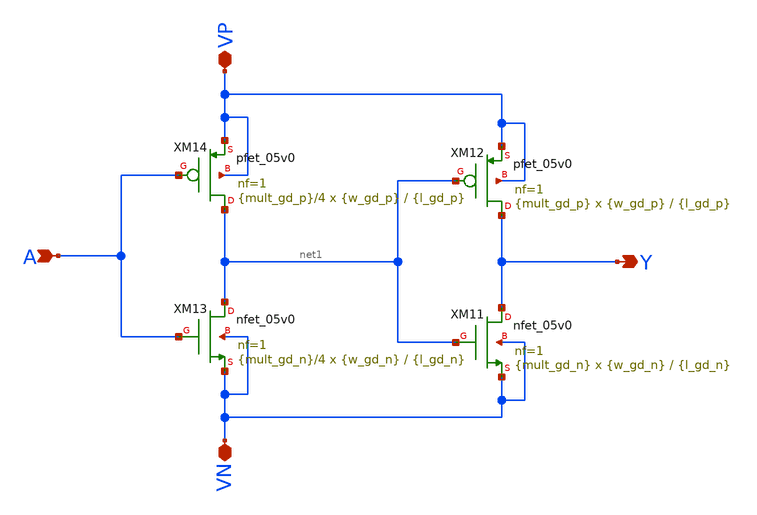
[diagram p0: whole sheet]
** sch_path: xschem/pwr_stage/GD_schem.sch
**.subckt GD_schem A VP VN Y
*.ipin A
*.iopin VP
*.iopin VN
*.opin Y
XM11 Y net1 VN VN nfet_05v0 L={l_gd_n} W={w_gd_n} nf=1 ad='int((nf+1)/2) * W/nf * 0.18u' as='int((nf+2)/2) * W/nf * 0.18u'
+ pd='2*int((nf+1)/2) * (W/nf + 0.18u)' ps='2*int((nf+2)/2) * (W/nf + 0.18u)' nrd='0.18u / W' nrs='0.18u / W'
+ sa=0 sb=0 sd=0 m={mult_gd_n}
XM12 Y net1 VP VP pfet_05v0 L={l_gd_p} W={w_gd_p} nf=1 ad='int((nf+1)/2) * W/nf * 0.18u' as='int((nf+2)/2) * W/nf * 0.18u'
+ pd='2*int((nf+1)/2) * (W/nf + 0.18u)' ps='2*int((nf+2)/2) * (W/nf + 0.18u)' nrd='0.18u / W' nrs='0.18u / W'
+ sa=0 sb=0 sd=0 m={mult_gd_p}
XM13 net1 A VN VN nfet_05v0 L={l_gd_n} W={w_gd_n} nf=1 ad='int((nf+1)/2) * W/nf * 0.18u' as='int((nf+2)/2) * W/nf * 0.18u'
+ pd='2*int((nf+1)/2) * (W/nf + 0.18u)' ps='2*int((nf+2)/2) * (W/nf + 0.18u)' nrd='0.18u / W' nrs='0.18u / W'
+ sa=0 sb=0 sd=0 m={mult_gd_n}/4
XM14 net1 A VP VP pfet_05v0 L={l_gd_p} W={w_gd_p} nf=1 ad='int((nf+1)/2) * W/nf * 0.18u' as='int((nf+2)/2) * W/nf * 0.18u'
+ pd='2*int((nf+1)/2) * (W/nf + 0.18u)' ps='2*int((nf+2)/2) * (W/nf + 0.18u)' nrd='0.18u / W' nrs='0.18u / W'
+ sa=0 sb=0 sd=0 m={mult_gd_p}/4
**.ends
.end
